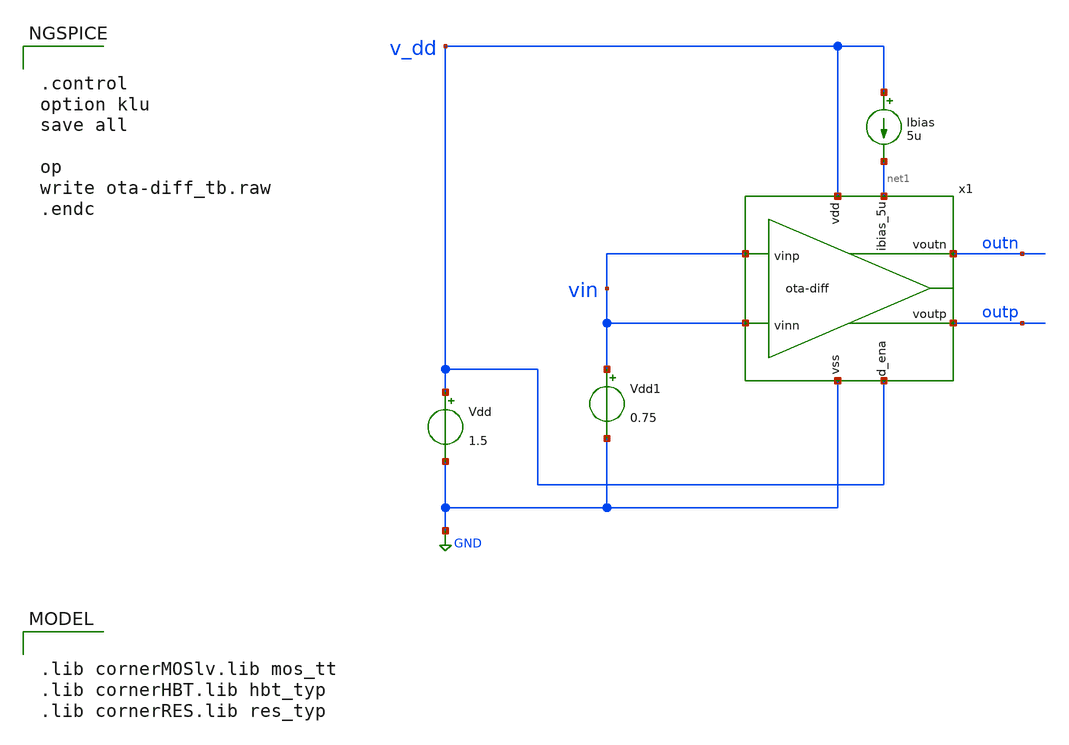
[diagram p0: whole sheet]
** sch_path: xschem/ota-diff_tb.sch
* (c) 2025 H. Pretl, Apache-2.0 license
* xschem/ota-diff.sch:
* (c) 2024 H. Pretl, Apache-2.0 license
**.subckt ota-diff_tb
Vdd v_dd GND 1.5
.save i(vdd)
x1 v_dd outp vin vin net1 v_dd GND outn ota-diff
Vdd1 vin GND 0.75
Ibias v_dd net1 5u
**** begin user architecture code

.lib cornerMOSlv.lib mos_tt
.lib cornerHBT.lib hbt_typ
.lib cornerRES.lib res_typ



.control
option klu
save all

op
write ota-diff_tb.raw
.endc


**** end user architecture code
**.ends

* expanding   symbol:  ota-diff.sym # of pins=8
** sym_path: xschem/ota-diff.sym
** sch_path: xschem/ota-diff.sch
.subckt ota-diff vdd voutp vinp vinn ibias_5u d_ena vss voutn
*.ipin ibias_5u
*.iopin vdd
*.iopin vss
*.ipin vinp
*.ipin vinn
*.ipin d_ena
*.opin voutp
*.opin voutn
XM7 vs vinp net1 vss sg13_lv_nmos w=10u l=0.5u ng=2 m=1 mm_ok=1
XM10 vs vinn net2 vss sg13_lv_nmos w=10u l=0.5u ng=2 m=1 mm_ok=1
XM11 vss ibias_5u net14 vss sg13_lv_nmos w=20u l=1u ng=2 m=1 mm_ok=1
XM15 voutp net1 vdd vdd sg13_lv_pmos w=100u l=0.5u ng=20 m=1 mm_ok=1
XM17 vss net3 net4 vss sg13_lv_nmos w=10u l=1u ng=1 m=1 mm_ok=1
XM19 vss ibias_5u ibias_5u vss sg13_lv_nmos w=10u l=10u ng=1 m=1 mm_ok=1
XMpd12 vss net7 ibias_5u vss sg13_lv_nmos w=1u l=0.13u ng=1 m=1 mm_ok=1
XMpd13 ibias_5u net8 ibias_5u vss sg13_lv_nmos w=1u l=0.13u ng=1 m=1 mm_ok=1
XR15 vg2 net9 sub! rhigh w=0.5e-6 l=20e-6 m=1 b=0 mm_ok=1
C1 net5 voutp 0.5p m=1
XR17 net1 net5 sub! rhigh w=0.5e-6 l=0.5e-6 m=1 b=0 mm_ok=1
C2 net6 voutn 0.5p m=1
XR18 net2 net6 sub! rhigh w=0.5e-6 l=0.5e-6 m=1 b=0 mm_ok=1
XMpd14 vss net7 net8 vss sg13_lv_nmos w=1u l=0.13u ng=1 m=1 mm_ok=1
XMpd15 net8 net7 vdd vdd sg13_lv_pmos w=1u l=0.13u ng=1 m=1 mm_ok=1
XMpd16 vss d_ena net7 vss sg13_lv_nmos w=1u l=0.13u ng=1 m=1 mm_ok=1
XMpd17 net7 d_ena vdd vdd sg13_lv_pmos w=1u l=0.13u ng=1 m=1 mm_ok=1
XR1 net9 net4 sub! rhigh w=0.5e-6 l=20e-6 m=1 b=0 mm_ok=1
XR2 net10 vg2 sub! rhigh w=0.5e-6 l=20e-6 m=1 b=0 mm_ok=1
XR5 net11 net10 sub! rhigh w=0.5e-6 l=20e-6 m=1 b=0 mm_ok=1
XR4 net13 net2 sub! rhigh w=0.5e-6 l=20e-6 m=1 b=0 mm_ok=1
XR6 net12 vg1 sub! rhigh w=0.5e-6 l=20e-6 m=1 b=0 mm_ok=1
XR7 net13 vg1 sub! rhigh w=0.5e-6 l=20e-6 m=1 b=0 mm_ok=1
XR3 net1 net12 sub! rhigh w=0.5e-6 l=20e-6 m=1 b=0 mm_ok=1
XM2 vss ibias_5u net3 vss sg13_lv_nmos w=5u l=1u ng=1 m=1 mm_ok=1
Vmeas voutp net4 0
.save i(vmeas)
Vmeas1 vg2 net3 0
.save i(vmeas1)
Vmeas2 vs net14 0
.save i(vmeas2)
Vmeas3 voutn net11 0
.save i(vmeas3)
XM3 voutn net2 vdd vdd sg13_lv_pmos w=100u l=0.5u ng=20 m=1 mm_ok=1
XM4 net2 vg1 vdd vdd sg13_lv_pmos w=100u l=0.5u ng=20 m=1 mm_ok=1
XM5 net1 vg1 vdd vdd sg13_lv_pmos w=100u l=0.5u ng=20 m=1 mm_ok=1
XM1 vss net3 net11 vss sg13_lv_nmos w=10u l=1u ng=1 m=1 mm_ok=1
.ends

.GLOBAL GND
.end
